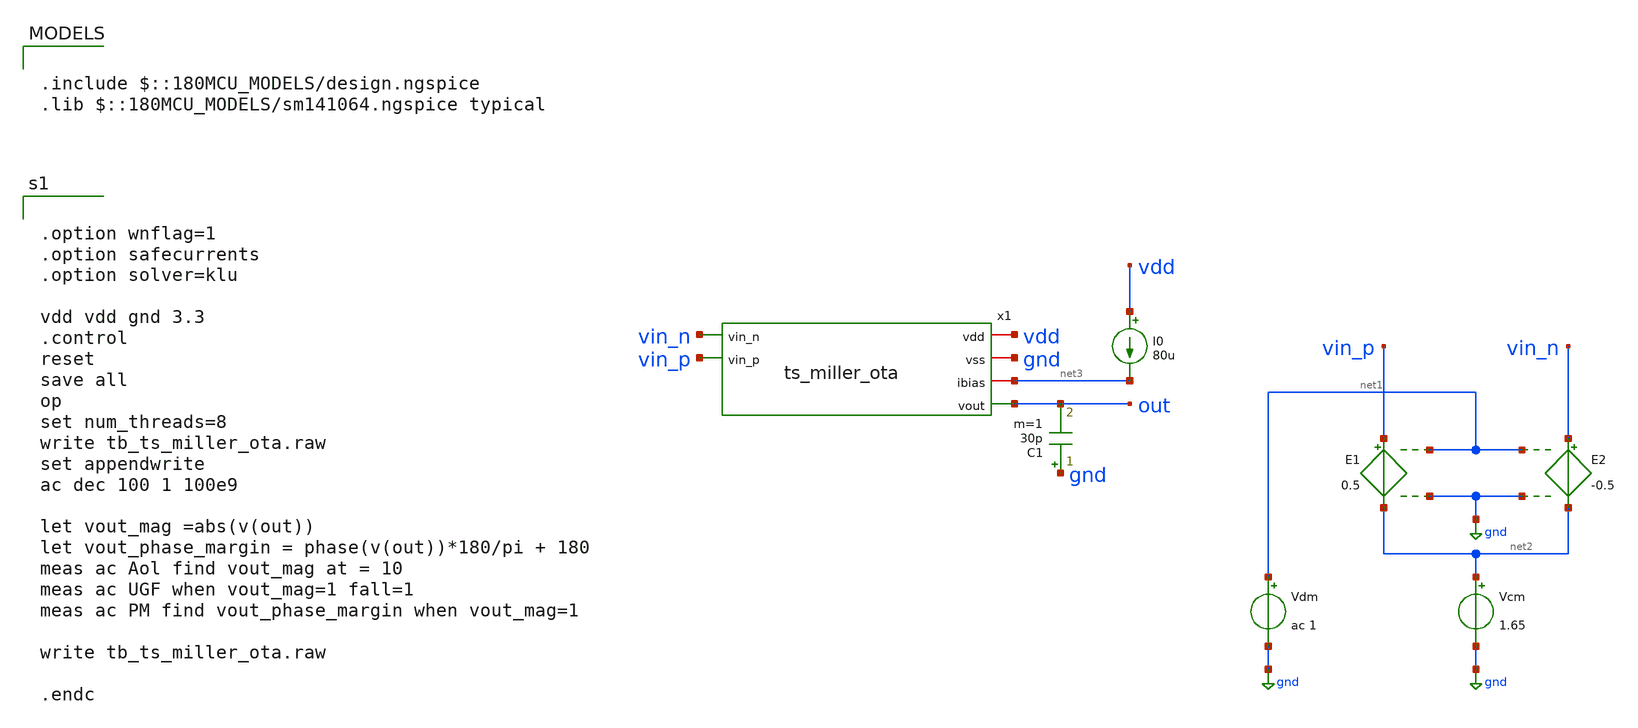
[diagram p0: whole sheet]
** sch_path: designs/libs/tb_analog/tb_ts_miller_ota/tb_ts_miller_ota.sch
**.subckt tb_ts_miller_ota
E1 vin_p net2 net1 gnd 0.5
E2 vin_n net2 net1 gnd -0.5
Vdm net1 gnd ac 1
Vcm net2 gnd 1.65
I0 vdd net3 80u
C1 gnd out 30p m=1
x1 vdd gnd net3 vin_n vin_p out ts_miller_ota
**** begin user architecture code


.option wnflag=1
.option safecurrents
.option solver=klu

vdd vdd gnd 3.3
.control
reset
save all
op
set num_threads=8
write tb_ts_miller_ota.raw
set appendwrite
ac dec 100 1 100e9

let vout_mag =abs(v(out))
let vout_phase_margin = phase(v(out))*180/pi + 180
meas ac Aol find vout_mag at = 10
meas ac UGF when vout_mag=1 fall=1
meas ac PM find vout_phase_margin when vout_mag=1

write tb_ts_miller_ota.raw

.endc



.include $::180MCU_MODELS/design.ngspice
.lib $::180MCU_MODELS/sm141064.ngspice typical

**** end user architecture code
**.ends
.GLOBAL gnd
.end
